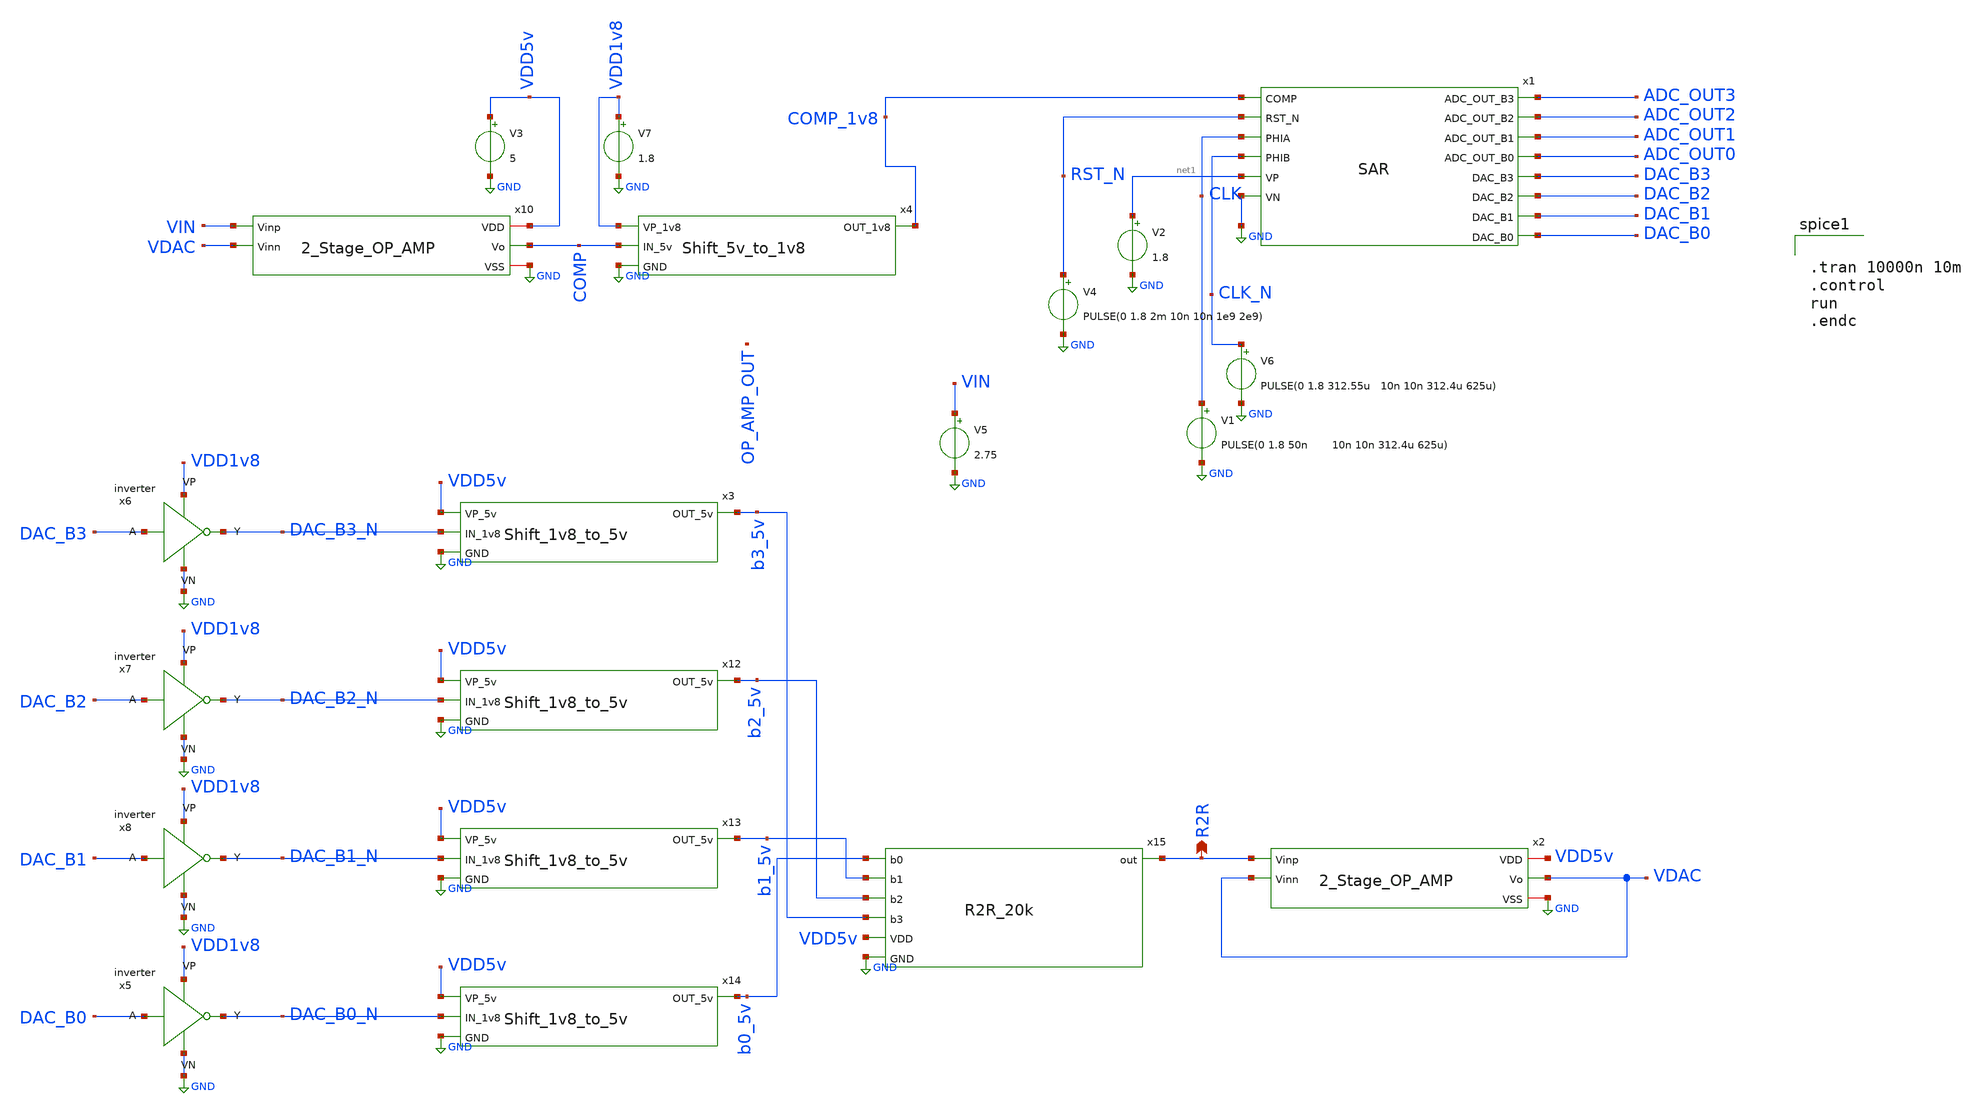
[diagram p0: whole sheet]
** sch_path: ADC/16bit_C2C/MagicAndSpice/EE431_FinalProj/SAR_tb.sch
**.subckt SAR_tb R2R
*.opin R2R
V1 CLK GND PULSE(0 1.8 50n 10n 10n 312.4u 625u)
V2 net1 GND 1.8
V4 RST_N GND PULSE(0 1.8 2m 10n 10n 1e9 2e9)
V5 VIN GND 2.75
V6 CLK_N GND PULSE(0 1.8 312.55u 10n 10n 312.4u 625u)
V3 VDD5v GND 5
V7 VDD1v8 GND 1.8
x10 VDD5v VIN VDAC COMP GND 2_Stage_OP_AMP
x2 VDD5v R2R VDAC VDAC GND 2_Stage_OP_AMP
x4 VDD1v8 COMP_1v8 COMP GND Shift_5v_to_1v8
x3 VDD5v b3_5v DAC_B3_N GND Shift_1v8_to_5v
x12 VDD5v b2_5v DAC_B2_N GND Shift_1v8_to_5v
x13 VDD5v b1_5v DAC_B1_N GND Shift_1v8_to_5v
x14 VDD5v b0_5v DAC_B0_N GND Shift_1v8_to_5v
x15 R2R b1_5v b2_5v b3_5v b0_5v VDD5v GND R2R_20k
x5 DAC_B0 DAC_B0_N VDD1v8 GND inverter
x8 DAC_B1 DAC_B1_N VDD1v8 GND inverter
x7 DAC_B2 DAC_B2_N VDD1v8 GND inverter
x6 DAC_B3 DAC_B3_N VDD1v8 GND inverter
x1 COMP_1v8 RST_N CLK CLK_N ADC_OUT3 ADC_OUT2 ADC_OUT1 ADC_OUT0 DAC_B3 DAC_B2 DAC_B1 DAC_B0 net1 GND
+ SAR
**** begin user architecture code
 .lib $::SKYWATER_MODELS/sky130.lib.spice tt


.tran 10000n 10m
.control
run
.endc

**** end user architecture code
**.ends
.GLOBAL GND
.end
